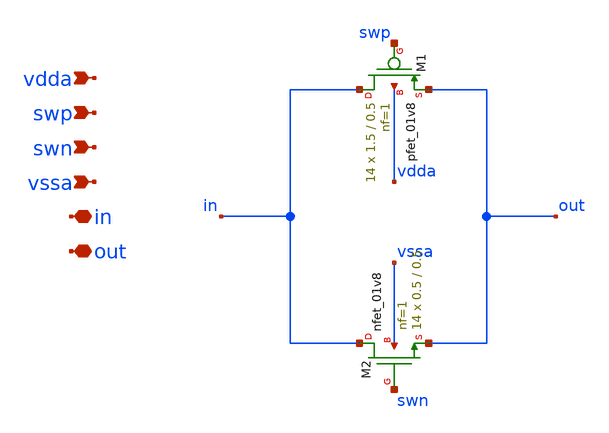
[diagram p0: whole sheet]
** sch_path: xschem/tg_sw_4.sch
**.subckt tg_sw_4 vdda swp swn vssa in out
*.ipin vdda
*.ipin swp
*.ipin swn
*.ipin vssa
*.iopin in
*.iopin out
XM1 in swp out vdda sky130_fd_pr__pfet_01v8 L=0.5 W=1.5 nf=1 ad='int((nf+1)/2) * W/nf * 0.29' as='int((nf+2)/2) * W/nf * 0.29'
+ pd='2*int((nf+1)/2) * (W/nf + 0.29)' ps='2*int((nf+2)/2) * (W/nf + 0.29)' nrd='0.29 / W' nrs='0.29 / W'
+ sa=0 sb=0 sd=0 mult=14 m=14
XM2 in swn out vssa sky130_fd_pr__nfet_01v8 L=0.5 W=0.5 nf=1 ad='int((nf+1)/2) * W/nf * 0.29' as='int((nf+2)/2) * W/nf * 0.29'
+ pd='2*int((nf+1)/2) * (W/nf + 0.29)' ps='2*int((nf+2)/2) * (W/nf + 0.29)' nrd='0.29 / W' nrs='0.29 / W'
+ sa=0 sb=0 sd=0 mult=14 m=14
**.ends
.end
